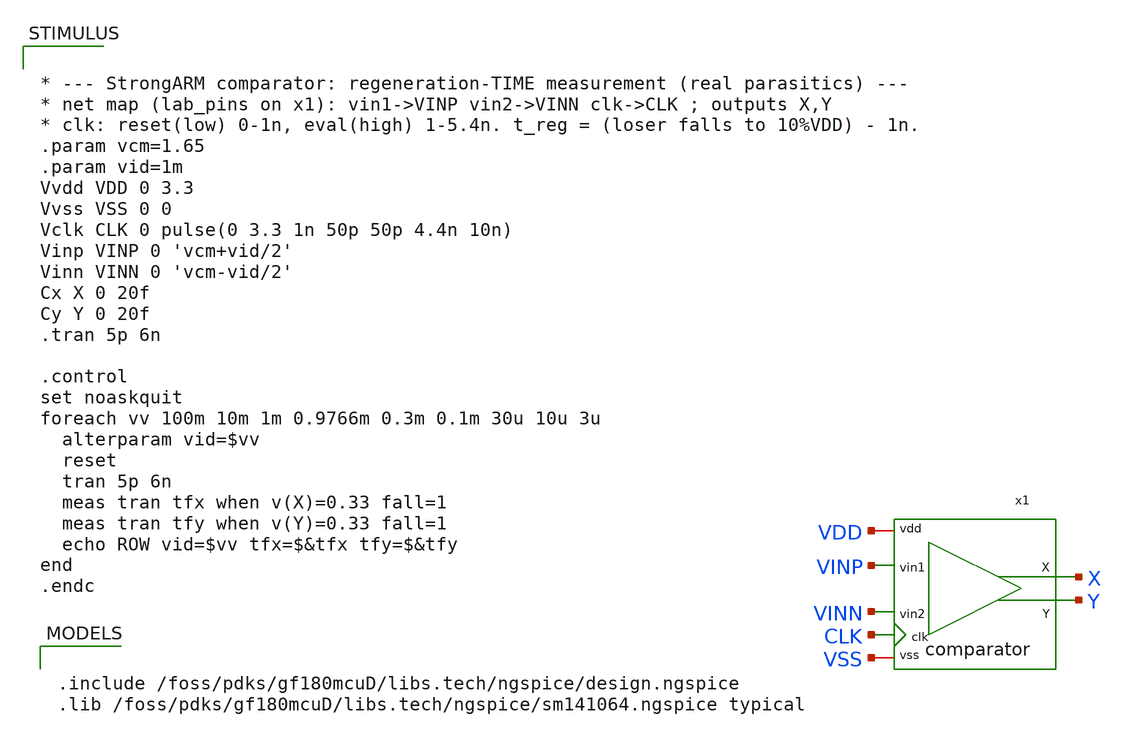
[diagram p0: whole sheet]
** sch_path: designs/libs/core_analog/saradc/tb/comparator_tb_regen.sch
**.subckt comparator_tb_regen
x1 VDD VSS X VINP Y VINN CLK comparator
**** begin user architecture code


.include /foss/pdks/gf180mcuD/libs.tech/ngspice/design.ngspice
.lib /foss/pdks/gf180mcuD/libs.tech/ngspice/sm141064.ngspice typical




* --- StrongARM comparator: regeneration-TIME measurement (real parasitics) ---
* net map (lab_pins on x1): vin1->VINP vin2->VINN clk->CLK ; outputs X,Y
* clk: reset(low) 0-1n, eval(high) 1-5.4n. t_reg = (loser falls to 10%VDD) - 1n.
.param vcm=1.65
.param vid=1m
Vvdd VDD 0 3.3
Vvss VSS 0 0
Vclk CLK 0 pulse(0 3.3 1n 50p 50p 4.4n 10n)
Vinp VINP 0 'vcm+vid/2'
Vinn VINN 0 'vcm-vid/2'
Cx X 0 20f
Cy Y 0 20f
.tran 5p 6n

.control
set noaskquit
foreach vv 100m 10m 1m 0.9766m 0.3m 0.1m 30u 10u 3u
  alterparam vid=$vv
  reset
  tran 5p 6n
  meas tran tfx when v(X)=0.33 fall=1
  meas tran tfy when v(Y)=0.33 fall=1
  echo ROW vid=$vv tfx=$&tfx tfy=$&tfy
end
.endc


**** end user architecture code
**.ends

* expanding   symbol:  comparator.sym # of pins=7
** sym_path: designs/libs/core_analog/saradc/comparator.sym
** sch_path: designs/libs/core_analog/saradc/comparator.sch
.subckt comparator vdd vss X vin1 Y vin2 clk
*.iopin vdd
*.iopin vss
*.ipin vin1
*.ipin vin2
*.ipin clk
*.opin X
*.opin Y
XM1 P vin1 net1 vss nfet_03v3 L=0.5u W=4u nf=4 ad='int((nf+1)/2) * W/nf * 0.18u' as='int((nf+2)/2) * W/nf * 0.18u'
+ pd='2*int((nf+1)/2) * (W/nf + 0.18u)' ps='2*int((nf+2)/2) * (W/nf + 0.18u)' nrd='0.18u / W' nrs='0.18u / W'
+ sa=0 sb=0 sd=0 m=1
XM2 Q vin2 net1 vss nfet_03v3 L=0.5u W=4u nf=4 ad='int((nf+1)/2) * W/nf * 0.18u' as='int((nf+2)/2) * W/nf * 0.18u'
+ pd='2*int((nf+1)/2) * (W/nf + 0.18u)' ps='2*int((nf+2)/2) * (W/nf + 0.18u)' nrd='0.18u / W' nrs='0.18u / W'
+ sa=0 sb=0 sd=0 m=1
XM3 X Y P vss nfet_03v3 L=0.28u W=2u nf=2 ad='int((nf+1)/2) * W/nf * 0.18u' as='int((nf+2)/2) * W/nf * 0.18u'
+ pd='2*int((nf+1)/2) * (W/nf + 0.18u)' ps='2*int((nf+2)/2) * (W/nf + 0.18u)' nrd='0.18u / W' nrs='0.18u / W'
+ sa=0 sb=0 sd=0 m=1
XM4 Y X Q vss nfet_03v3 L=0.28u W=2u nf=2 ad='int((nf+1)/2) * W/nf * 0.18u' as='int((nf+2)/2) * W/nf * 0.18u'
+ pd='2*int((nf+1)/2) * (W/nf + 0.18u)' ps='2*int((nf+2)/2) * (W/nf + 0.18u)' nrd='0.18u / W' nrs='0.18u / W'
+ sa=0 sb=0 sd=0 m=1
XM5 X Y vdd vdd pfet_03v3 L=0.28u W=6u nf=2 ad='int((nf+1)/2) * W/nf * 0.18u' as='int((nf+2)/2) * W/nf * 0.18u'
+ pd='2*int((nf+1)/2) * (W/nf + 0.18u)' ps='2*int((nf+2)/2) * (W/nf + 0.18u)' nrd='0.18u / W' nrs='0.18u / W'
+ sa=0 sb=0 sd=0 m=1
XM6 Y X vdd vdd pfet_03v3 L=0.28u W=6u nf=2 ad='int((nf+1)/2) * W/nf * 0.18u' as='int((nf+2)/2) * W/nf * 0.18u'
+ pd='2*int((nf+1)/2) * (W/nf + 0.18u)' ps='2*int((nf+2)/2) * (W/nf + 0.18u)' nrd='0.18u / W' nrs='0.18u / W'
+ sa=0 sb=0 sd=0 m=1
XM7 net1 clk vss vss nfet_03v3 L=0.28u W=6u nf=4 ad='int((nf+1)/2) * W/nf * 0.18u' as='int((nf+2)/2) * W/nf * 0.18u'
+ pd='2*int((nf+1)/2) * (W/nf + 0.18u)' ps='2*int((nf+2)/2) * (W/nf + 0.18u)' nrd='0.18u / W' nrs='0.18u / W'
+ sa=0 sb=0 sd=0 m=1
XM8 X clk vdd vdd pfet_03v3 L=0.28u W=2u nf=1 ad='int((nf+1)/2) * W/nf * 0.18u' as='int((nf+2)/2) * W/nf * 0.18u'
+ pd='2*int((nf+1)/2) * (W/nf + 0.18u)' ps='2*int((nf+2)/2) * (W/nf + 0.18u)' nrd='0.18u / W' nrs='0.18u / W'
+ sa=0 sb=0 sd=0 m=1
XM9 P clk vdd vdd pfet_03v3 L=0.28u W=2u nf=1 ad='int((nf+1)/2) * W/nf * 0.18u' as='int((nf+2)/2) * W/nf * 0.18u'
+ pd='2*int((nf+1)/2) * (W/nf + 0.18u)' ps='2*int((nf+2)/2) * (W/nf + 0.18u)' nrd='0.18u / W' nrs='0.18u / W'
+ sa=0 sb=0 sd=0 m=1
XM10 Y clk vdd vdd pfet_03v3 L=0.28u W=2u nf=1 ad='int((nf+1)/2) * W/nf * 0.18u' as='int((nf+2)/2) * W/nf * 0.18u'
+ pd='2*int((nf+1)/2) * (W/nf + 0.18u)' ps='2*int((nf+2)/2) * (W/nf + 0.18u)' nrd='0.18u / W' nrs='0.18u / W'
+ sa=0 sb=0 sd=0 m=1
XM11 Q clk vdd vdd pfet_03v3 L=0.28u W=2u nf=1 ad='int((nf+1)/2) * W/nf * 0.18u' as='int((nf+2)/2) * W/nf * 0.18u'
+ pd='2*int((nf+1)/2) * (W/nf + 0.18u)' ps='2*int((nf+2)/2) * (W/nf + 0.18u)' nrd='0.18u / W' nrs='0.18u / W'
+ sa=0 sb=0 sd=0 m=1
.ends

.end
